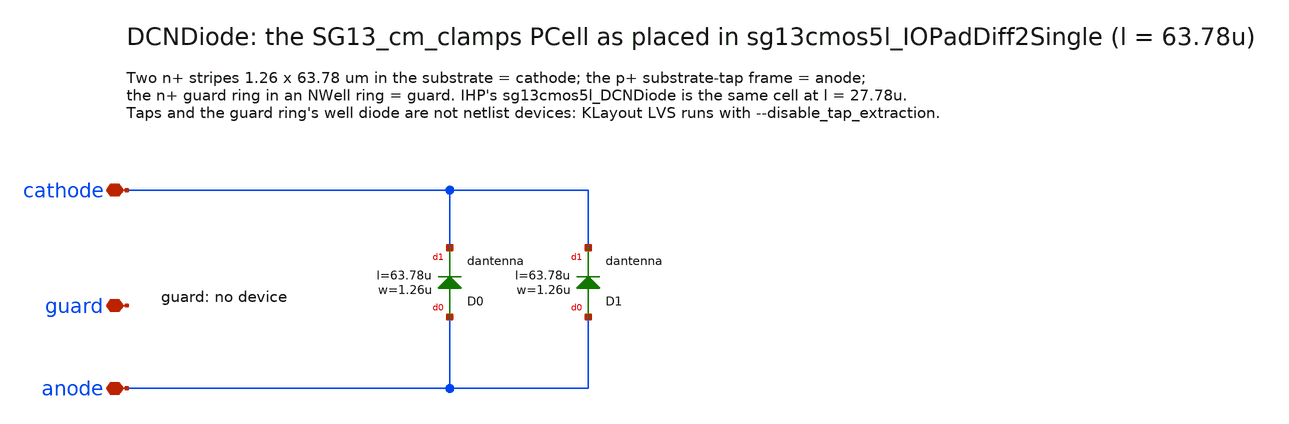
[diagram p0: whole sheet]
** sch_path: macros/IOPad/schematic/xschem/DCNDiode.sch
**.subckt DCNDiode anode cathode guard
*.iopin anode
*.iopin cathode
*.iopin guard
XD0 anode cathode dantenna l=63.78u w=1.26u
XD1 anode cathode dantenna l=63.78u w=1.26u
**.ends
.end
